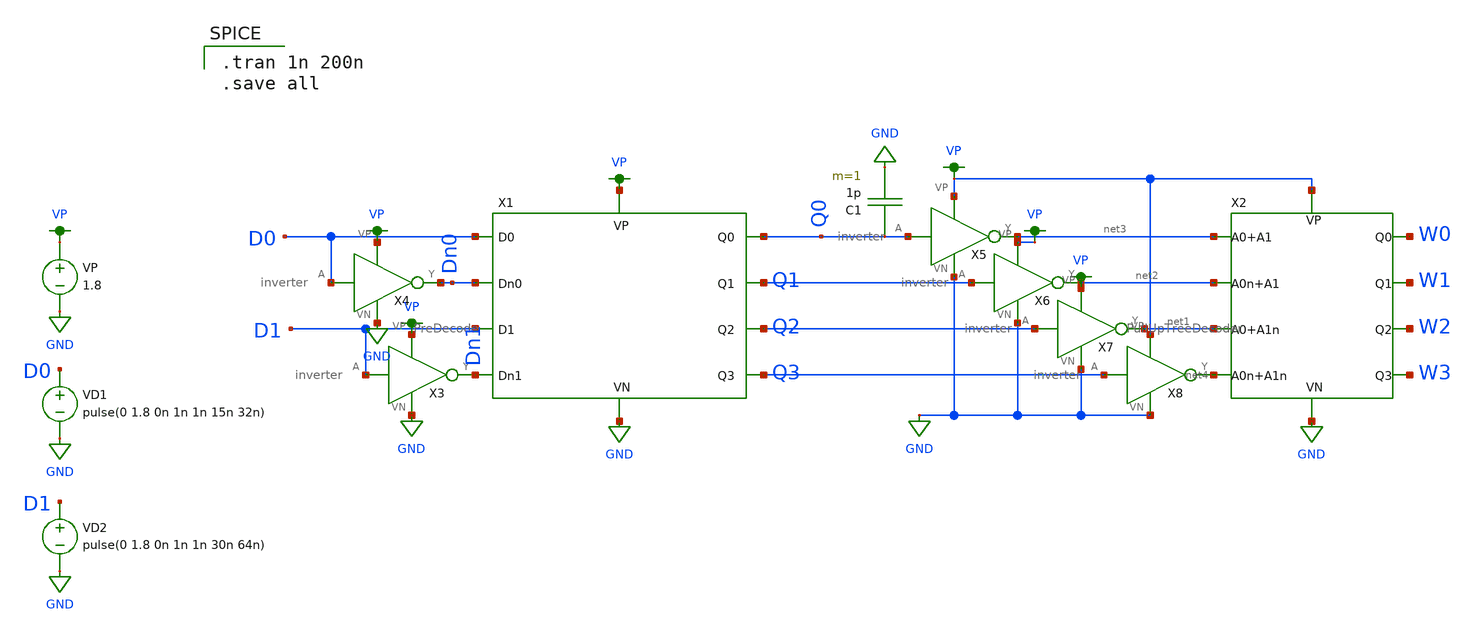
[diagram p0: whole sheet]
** sch_path: DRAM_Components/Schematic/DecoderSim.sch
**.subckt DecoderSim
VP VP GND 1.8
VD1 D0 GND pulse(0 1.8 0n 1n 1n 15n 32n)
X1 Q0 VP GND Q1 Q2 Q3 Dn1 D1 Dn0 D0 PreDecode
X3 D1 Dn1 VP GND inverter
X4 D0 Dn0 VP GND inverter
VD2 D1 GND pulse(0 1.8 0n 1n 1n 30n 64n)
X2 W0 VP GND W1 W2 W3 net4 net1 net2 net3 PullUpTreeDecoder
X5 Q0 net3 VP GND inverter
X6 Q1 net2 VP GND inverter
X7 Q2 net1 VP GND inverter
X8 Q3 net4 VP GND inverter
C1 Q0 GND 1p m=1
**** begin user architecture code

.option wnflag=1
.param MC_SWITCH=0.0
.lib ~/skywater/skywater-pdk/libraries/sky130_fd_pr_ngspice/latest/models/sky130.lib.spice tt


.tran 1n 200n
.save all

**** end user architecture code
**.ends

* expanding   symbol:  /home/madvlsi/Desktop/CMOSDRAM/DRAM_Components/Schematic/PreDecode.sym # of
*+ pins=10
** sym_path: DRAM_Components/Schematic/PreDecode.sym
** sch_path: DRAM_Components/Schematic/PreDecode.sch
.subckt PreDecode Q0 VP VN Q1 Q2 Q3 A1n A1 A0n A0
*.ipin A0
*.ipin A0n
*.ipin A1
*.ipin A1n
*.opin Q0
*.opin Q1
*.opin Q2
*.opin Q3
*.iopin VP
*.iopin VN
XM2 net1 A1n VP VP sky130_fd_pr__pfet_01v8 L=0.15 W=2 nf=1 ad='int((nf+1)/2) * W/nf * 0.29' as='int((nf+2)/2) * W/nf * 0.29'
+ pd='2*int((nf+1)/2) * (W/nf + 0.29)' ps='2*int((nf+2)/2) * (W/nf + 0.29)' nrd='0.29 / W' nrs='0.29 / W'
+ sa=0 sb=0 sd=0 mult=1 m=1
XM1 net2 A1 VP VP sky130_fd_pr__pfet_01v8 L=0.15 W=2 nf=1 ad='int((nf+1)/2) * W/nf * 0.29' as='int((nf+2)/2) * W/nf * 0.29'
+ pd='2*int((nf+1)/2) * (W/nf + 0.29)' ps='2*int((nf+2)/2) * (W/nf + 0.29)' nrd='0.29 / W' nrs='0.29 / W'
+ sa=0 sb=0 sd=0 mult=1 m=1
XM3 net2 VP VP VP sky130_fd_pr__pfet_01v8 L=0.15 W=2 nf=1 ad='int((nf+1)/2) * W/nf * 0.29' as='int((nf+2)/2) * W/nf * 0.29'
+ pd='2*int((nf+1)/2) * (W/nf + 0.29)' ps='2*int((nf+2)/2) * (W/nf + 0.29)' nrd='0.29 / W' nrs='0.29 / W'
+ sa=0 sb=0 sd=0 mult=1 m=1
XM4 net1 VP VP VP sky130_fd_pr__pfet_01v8 L=0.15 W=2 nf=1 ad='int((nf+1)/2) * W/nf * 0.29' as='int((nf+2)/2) * W/nf * 0.29'
+ pd='2*int((nf+1)/2) * (W/nf + 0.29)' ps='2*int((nf+2)/2) * (W/nf + 0.29)' nrd='0.29 / W' nrs='0.29 / W'
+ sa=0 sb=0 sd=0 mult=1 m=1
XM5 Q1 A0n net2 VP sky130_fd_pr__pfet_01v8 L=0.15 W=1 nf=1 ad='int((nf+1)/2) * W/nf * 0.29' as='int((nf+2)/2) * W/nf * 0.29'
+ pd='2*int((nf+1)/2) * (W/nf + 0.29)' ps='2*int((nf+2)/2) * (W/nf + 0.29)' nrd='0.29 / W' nrs='0.29 / W'
+ sa=0 sb=0 sd=0 mult=1 m=1
XM6 Q0 A0 net2 VP sky130_fd_pr__pfet_01v8 L=0.15 W=1 nf=1 ad='int((nf+1)/2) * W/nf * 0.29' as='int((nf+2)/2) * W/nf * 0.29'
+ pd='2*int((nf+1)/2) * (W/nf + 0.29)' ps='2*int((nf+2)/2) * (W/nf + 0.29)' nrd='0.29 / W' nrs='0.29 / W'
+ sa=0 sb=0 sd=0 mult=1 m=1
XM7 Q2 A0 net1 VP sky130_fd_pr__pfet_01v8 L=0.15 W=1 nf=1 ad='int((nf+1)/2) * W/nf * 0.29' as='int((nf+2)/2) * W/nf * 0.29'
+ pd='2*int((nf+1)/2) * (W/nf + 0.29)' ps='2*int((nf+2)/2) * (W/nf + 0.29)' nrd='0.29 / W' nrs='0.29 / W'
+ sa=0 sb=0 sd=0 mult=1 m=1
XM8 Q3 A0n net1 VP sky130_fd_pr__pfet_01v8 L=0.15 W=1 nf=1 ad='int((nf+1)/2) * W/nf * 0.29' as='int((nf+2)/2) * W/nf * 0.29'
+ pd='2*int((nf+1)/2) * (W/nf + 0.29)' ps='2*int((nf+2)/2) * (W/nf + 0.29)' nrd='0.29 / W' nrs='0.29 / W'
+ sa=0 sb=0 sd=0 mult=1 m=1
XM9 VN A0 Q0 VN sky130_fd_pr__nfet_01v8 L=0.15 W=1 nf=1 ad='int((nf+1)/2) * W/nf * 0.29' as='int((nf+2)/2) * W/nf * 0.29'
+ pd='2*int((nf+1)/2) * (W/nf + 0.29)' ps='2*int((nf+2)/2) * (W/nf + 0.29)' nrd='0.29 / W' nrs='0.29 / W'
+ sa=0 sb=0 sd=0 mult=1 m=1
XM10 VN A0n Q1 VN sky130_fd_pr__nfet_01v8 L=0.15 W=1 nf=1 ad='int((nf+1)/2) * W/nf * 0.29' as='int((nf+2)/2) * W/nf * 0.29'
+ pd='2*int((nf+1)/2) * (W/nf + 0.29)' ps='2*int((nf+2)/2) * (W/nf + 0.29)' nrd='0.29 / W' nrs='0.29 / W'
+ sa=0 sb=0 sd=0 mult=1 m=1
XM11 VN A1 Q0 VN sky130_fd_pr__nfet_01v8 L=0.15 W=1 nf=1 ad='int((nf+1)/2) * W/nf * 0.29' as='int((nf+2)/2) * W/nf * 0.29'
+ pd='2*int((nf+1)/2) * (W/nf + 0.29)' ps='2*int((nf+2)/2) * (W/nf + 0.29)' nrd='0.29 / W' nrs='0.29 / W'
+ sa=0 sb=0 sd=0 mult=1 m=1
XM12 VN A1 Q1 VN sky130_fd_pr__nfet_01v8 L=0.15 W=1 nf=1 ad='int((nf+1)/2) * W/nf * 0.29' as='int((nf+2)/2) * W/nf * 0.29'
+ pd='2*int((nf+1)/2) * (W/nf + 0.29)' ps='2*int((nf+2)/2) * (W/nf + 0.29)' nrd='0.29 / W' nrs='0.29 / W'
+ sa=0 sb=0 sd=0 mult=1 m=1
XM13 VN A0 Q2 VN sky130_fd_pr__nfet_01v8 L=0.15 W=1 nf=1 ad='int((nf+1)/2) * W/nf * 0.29' as='int((nf+2)/2) * W/nf * 0.29'
+ pd='2*int((nf+1)/2) * (W/nf + 0.29)' ps='2*int((nf+2)/2) * (W/nf + 0.29)' nrd='0.29 / W' nrs='0.29 / W'
+ sa=0 sb=0 sd=0 mult=1 m=1
XM14 VN A0n Q3 VN sky130_fd_pr__nfet_01v8 L=0.15 W=1 nf=1 ad='int((nf+1)/2) * W/nf * 0.29' as='int((nf+2)/2) * W/nf * 0.29'
+ pd='2*int((nf+1)/2) * (W/nf + 0.29)' ps='2*int((nf+2)/2) * (W/nf + 0.29)' nrd='0.29 / W' nrs='0.29 / W'
+ sa=0 sb=0 sd=0 mult=1 m=1
XM15 VN A1n Q2 VN sky130_fd_pr__nfet_01v8 L=0.15 W=1 nf=1 ad='int((nf+1)/2) * W/nf * 0.29' as='int((nf+2)/2) * W/nf * 0.29'
+ pd='2*int((nf+1)/2) * (W/nf + 0.29)' ps='2*int((nf+2)/2) * (W/nf + 0.29)' nrd='0.29 / W' nrs='0.29 / W'
+ sa=0 sb=0 sd=0 mult=1 m=1
XM16 VN A1n Q3 VN sky130_fd_pr__nfet_01v8 L=0.15 W=1 nf=1 ad='int((nf+1)/2) * W/nf * 0.29' as='int((nf+2)/2) * W/nf * 0.29'
+ pd='2*int((nf+1)/2) * (W/nf + 0.29)' ps='2*int((nf+2)/2) * (W/nf + 0.29)' nrd='0.29 / W' nrs='0.29 / W'
+ sa=0 sb=0 sd=0 mult=1 m=1
.ends


* expanding   symbol:  /home/madvlsi/Desktop/CMOSDRAM/DRAM_Components/Schematic/inverter.sym # of
*+ pins=4
** sym_path: DRAM_Components/Schematic/inverter.sym
** sch_path: DRAM_Components/Schematic/inverter.sch
.subckt inverter A Y VP VN
*.ipin A
*.iopin VP
*.opin Y
*.iopin VN
XM1 Y A VP VP sky130_fd_pr__pfet_01v8 L=0.15 W=1 nf=1 ad='int((nf+1)/2) * W/nf * 0.29' as='int((nf+2)/2) * W/nf * 0.29'
+ pd='2*int((nf+1)/2) * (W/nf + 0.29)' ps='2*int((nf+2)/2) * (W/nf + 0.29)' nrd='0.29 / W' nrs='0.29 / W'
+ sa=0 sb=0 sd=0 mult=1 m=1
XM2 Y A VN VN sky130_fd_pr__nfet_01v8 L=0.15 W=1 nf=1 ad='int((nf+1)/2) * W/nf * 0.29' as='int((nf+2)/2) * W/nf * 0.29'
+ pd='2*int((nf+1)/2) * (W/nf + 0.29)' ps='2*int((nf+2)/2) * (W/nf + 0.29)' nrd='0.29 / W' nrs='0.29 / W'
+ sa=0 sb=0 sd=0 mult=1 m=1
.ends


* expanding   symbol:
*+  /home/madvlsi/Desktop/CMOSDRAM/DRAM_Components/Schematic/PullUpTreeDecoder.sym # of pins=10
** sym_path: DRAM_Components/Schematic/PullUpTreeDecoder.sym
** sch_path: DRAM_Components/Schematic/PullUpTreeDecoder.sch
.subckt PullUpTreeDecoder Q0 VP VN Q1 Q2 Q3 A0nA1n A0A1n A0nA1 A0A1
*.iopin VP
*.iopin VN
*.ipin A0A1
*.ipin A0nA1
*.ipin A0A1n
*.ipin A0nA1n
*.opin Q0
*.opin Q1
*.opin Q2
*.opin Q3
XM2 Q0 A0A1 VN VN sky130_fd_pr__nfet_01v8 L=0.15 W=2 nf=1 ad='int((nf+1)/2) * W/nf * 0.29' as='int((nf+2)/2) * W/nf * 0.29'
+ pd='2*int((nf+1)/2) * (W/nf + 0.29)' ps='2*int((nf+2)/2) * (W/nf + 0.29)' nrd='0.29 / W' nrs='0.29 / W'
+ sa=0 sb=0 sd=0 mult=1 m=1
XM3 Q1 A0nA1 VP VP sky130_fd_pr__pfet_01v8 L=0.15 W=4 nf=1 ad='int((nf+1)/2) * W/nf * 0.29' as='int((nf+2)/2) * W/nf * 0.29'
+ pd='2*int((nf+1)/2) * (W/nf + 0.29)' ps='2*int((nf+2)/2) * (W/nf + 0.29)' nrd='0.29 / W' nrs='0.29 / W'
+ sa=0 sb=0 sd=0 mult=1 m=1
XM4 Q0 A0A1 VP VP sky130_fd_pr__pfet_01v8 L=0.15 W=4 nf=1 ad='int((nf+1)/2) * W/nf * 0.29' as='int((nf+2)/2) * W/nf * 0.29'
+ pd='2*int((nf+1)/2) * (W/nf + 0.29)' ps='2*int((nf+2)/2) * (W/nf + 0.29)' nrd='0.29 / W' nrs='0.29 / W'
+ sa=0 sb=0 sd=0 mult=1 m=1
XM5 Q2 A0A1n VP VP sky130_fd_pr__pfet_01v8 L=0.15 W=4 nf=1 ad='int((nf+1)/2) * W/nf * 0.29' as='int((nf+2)/2) * W/nf * 0.29'
+ pd='2*int((nf+1)/2) * (W/nf + 0.29)' ps='2*int((nf+2)/2) * (W/nf + 0.29)' nrd='0.29 / W' nrs='0.29 / W'
+ sa=0 sb=0 sd=0 mult=1 m=1
XM6 Q3 A0nA1n VP VP sky130_fd_pr__pfet_01v8 L=0.15 W=4 nf=1 ad='int((nf+1)/2) * W/nf * 0.29' as='int((nf+2)/2) * W/nf * 0.29'
+ pd='2*int((nf+1)/2) * (W/nf + 0.29)' ps='2*int((nf+2)/2) * (W/nf + 0.29)' nrd='0.29 / W' nrs='0.29 / W'
+ sa=0 sb=0 sd=0 mult=1 m=1
XM7 Q1 A0nA1 VN VN sky130_fd_pr__nfet_01v8 L=0.15 W=2 nf=1 ad='int((nf+1)/2) * W/nf * 0.29' as='int((nf+2)/2) * W/nf * 0.29'
+ pd='2*int((nf+1)/2) * (W/nf + 0.29)' ps='2*int((nf+2)/2) * (W/nf + 0.29)' nrd='0.29 / W' nrs='0.29 / W'
+ sa=0 sb=0 sd=0 mult=1 m=1
XM8 Q2 A0A1n VN VN sky130_fd_pr__nfet_01v8 L=0.15 W=2 nf=1 ad='int((nf+1)/2) * W/nf * 0.29' as='int((nf+2)/2) * W/nf * 0.29'
+ pd='2*int((nf+1)/2) * (W/nf + 0.29)' ps='2*int((nf+2)/2) * (W/nf + 0.29)' nrd='0.29 / W' nrs='0.29 / W'
+ sa=0 sb=0 sd=0 mult=1 m=1
XM9 Q3 A0nA1n VN VN sky130_fd_pr__nfet_01v8 L=0.15 W=2 nf=1 ad='int((nf+1)/2) * W/nf * 0.29' as='int((nf+2)/2) * W/nf * 0.29'
+ pd='2*int((nf+1)/2) * (W/nf + 0.29)' ps='2*int((nf+2)/2) * (W/nf + 0.29)' nrd='0.29 / W' nrs='0.29 / W'
+ sa=0 sb=0 sd=0 mult=1 m=1
XM1 VP VP Q0 VP sky130_fd_pr__pfet_01v8 L=0.15 W=4 nf=1 ad='int((nf+1)/2) * W/nf * 0.29' as='int((nf+2)/2) * W/nf * 0.29'
+ pd='2*int((nf+1)/2) * (W/nf + 0.29)' ps='2*int((nf+2)/2) * (W/nf + 0.29)' nrd='0.29 / W' nrs='0.29 / W'
+ sa=0 sb=0 sd=0 mult=1 m=1
XM10 VN VN Q0 VN sky130_fd_pr__nfet_01v8 L=0.15 W=2 nf=1 ad='int((nf+1)/2) * W/nf * 0.29' as='int((nf+2)/2) * W/nf * 0.29'
+ pd='2*int((nf+1)/2) * (W/nf + 0.29)' ps='2*int((nf+2)/2) * (W/nf + 0.29)' nrd='0.29 / W' nrs='0.29 / W'
+ sa=0 sb=0 sd=0 mult=1 m=1
XM11 VN VN Q3 VN sky130_fd_pr__nfet_01v8 L=0.15 W=2 nf=1 ad='int((nf+1)/2) * W/nf * 0.29' as='int((nf+2)/2) * W/nf * 0.29'
+ pd='2*int((nf+1)/2) * (W/nf + 0.29)' ps='2*int((nf+2)/2) * (W/nf + 0.29)' nrd='0.29 / W' nrs='0.29 / W'
+ sa=0 sb=0 sd=0 mult=1 m=1
XM12 VN VN Q1 VN sky130_fd_pr__nfet_01v8 L=0.15 W=2 nf=1 ad='int((nf+1)/2) * W/nf * 0.29' as='int((nf+2)/2) * W/nf * 0.29'
+ pd='2*int((nf+1)/2) * (W/nf + 0.29)' ps='2*int((nf+2)/2) * (W/nf + 0.29)' nrd='0.29 / W' nrs='0.29 / W'
+ sa=0 sb=0 sd=0 mult=1 m=1
XM13 VN VN Q2 VN sky130_fd_pr__nfet_01v8 L=0.15 W=2 nf=1 ad='int((nf+1)/2) * W/nf * 0.29' as='int((nf+2)/2) * W/nf * 0.29'
+ pd='2*int((nf+1)/2) * (W/nf + 0.29)' ps='2*int((nf+2)/2) * (W/nf + 0.29)' nrd='0.29 / W' nrs='0.29 / W'
+ sa=0 sb=0 sd=0 mult=1 m=1
XM14 VP VP Q1 VP sky130_fd_pr__pfet_01v8 L=0.15 W=4 nf=1 ad='int((nf+1)/2) * W/nf * 0.29' as='int((nf+2)/2) * W/nf * 0.29'
+ pd='2*int((nf+1)/2) * (W/nf + 0.29)' ps='2*int((nf+2)/2) * (W/nf + 0.29)' nrd='0.29 / W' nrs='0.29 / W'
+ sa=0 sb=0 sd=0 mult=1 m=1
XM15 Q2 VP VP VP sky130_fd_pr__pfet_01v8 L=0.15 W=4 nf=1 ad='int((nf+1)/2) * W/nf * 0.29' as='int((nf+2)/2) * W/nf * 0.29'
+ pd='2*int((nf+1)/2) * (W/nf + 0.29)' ps='2*int((nf+2)/2) * (W/nf + 0.29)' nrd='0.29 / W' nrs='0.29 / W'
+ sa=0 sb=0 sd=0 mult=1 m=1
XM16 VP VP Q3 VP sky130_fd_pr__pfet_01v8 L=0.15 W=4 nf=1 ad='int((nf+1)/2) * W/nf * 0.29' as='int((nf+2)/2) * W/nf * 0.29'
+ pd='2*int((nf+1)/2) * (W/nf + 0.29)' ps='2*int((nf+2)/2) * (W/nf + 0.29)' nrd='0.29 / W' nrs='0.29 / W'
+ sa=0 sb=0 sd=0 mult=1 m=1
.ends

.GLOBAL GND
.GLOBAL VP
.end
